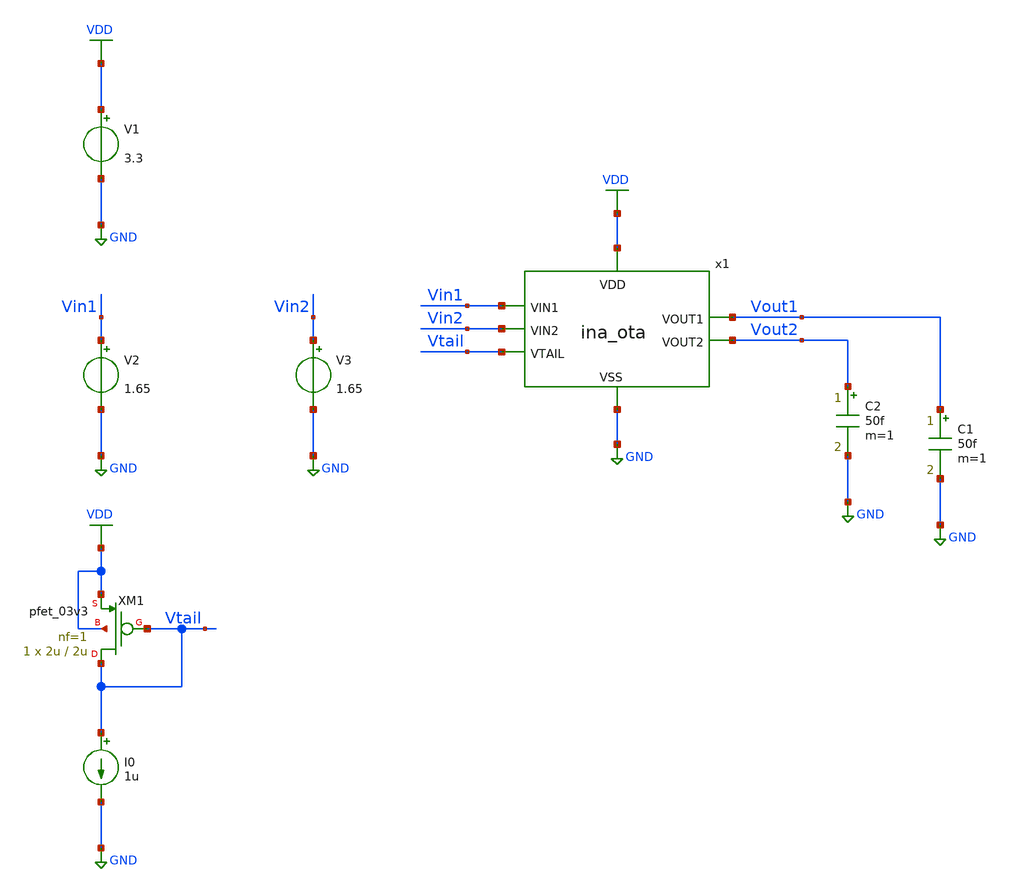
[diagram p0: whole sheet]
** sch_path: designs/libs/tb_ina/tb_ina_ota_ac/tb_ina_ota_ac.sch
**.subckt tb_ina_ota_ac
V1 VDD GND 3.3
V2 Vin1 GND 1.65
V3 Vin2 GND 1.65
C2 Vout2 GND 50f m=1
C1 Vout1 GND 50f m=1
XM1 Vtail Vtail VDD VDD pfet_03v3 L=2u W=2u nf=1 ad='int((nf+1)/2) * W/nf * 0.18u' as='int((nf+2)/2) * W/nf * 0.18u'
+ pd='2*int((nf+1)/2) * (W/nf + 0.18u)' ps='2*int((nf+2)/2) * (W/nf + 0.18u)' nrd='0.18u / W' nrs='0.18u / W'
+ sa=0 sb=0 sd=0 m=1
I0 Vtail GND 1u
x1 VDD Vtail Vin1 Vout2 Vout1 Vin2 GND ina_ota
**** begin user architecture code

.include $::180MCU_MODELS/design.ngspice
.lib $::180MCU_MODELS/sm141064.ngspice typical
.lib $::180MCU_MODELS/sm141064.ngspice cap_mim
.lib $::180MCU_MODELS/sm141064.ngspice moscap_typical
.lib $::180MCU_MODELS/sm141064.ngspice mimcap_typical
.lib $::180MCU_MODELS/sm141064.ngspice res_typical
* .lib $::180MCU_MODELS/sm141064.ngspice res_statistical
* ngspice commands




.control
save all

run
set color0 = white

*************************************
** PARAMETERS
*************************************

let Vdd  = 3.3
let Vcm  = 1.65
let Ibias = 1u

*************************************
** SOURCES
*************************************

alter @V1[DC] = $&Vdd
alter @V2[DC] = $&Vcm
alter @V3[DC] = $&Vcm
alter @V2[ACMAG] = 0.5
alter @V3[ACMAG] = -0.5
alter @I0[DC] = $&Ibias

*************************************
** AC SIMULATION
*************************************

ac dec 100 1 1G

*************************************
** MEASUREMENTS
*************************************

let vout_diff = v(Vout1)-v(Vout2)
let vin_diff  = v(Vin1)-v(Vin2)
let Av = vout_diff/vin_diff
let gain_db = db(Av)
let phase_deg = cph(Av)*180/pi
meas ac A0 FIND gain_db AT=1
let A0_3dB = A0 - 3
meas ac BW WHEN gain_db=A0_3dB
meas ac UGF WHEN gain_db=0
meas ac PHASE_UGF FIND phase_deg WHEN gain_db=0
let PM = PHASE_UGF
print PM

*************************************
** PLOTS
*************************************

plot gain_db
plot phase_deg

*************************************
** SAVE
*************************************

write tb_ina_ota_ac.raw


.endc
* ngspice commands



**** end user architecture code
**.ends

* expanding   symbol:  libs/core_ina/ina_ota/ina_ota.sym # of pins=7
** sym_path: designs/libs/core_ina/ina_ota/ina_ota.sym
** sch_path: designs/libs/core_ina/ina_ota/ina_ota.sch
.subckt ina_ota VDD VTAIL VIN1 VOUT2 VOUT1 VIN2 VSS
*.ipin Vin1
*.ipin Vin2
*.ipin Vtail
*.ipin VSS
*.opin Vout1
*.ipin VDD
*.opin Vout2
XM2 net4 net4 VDD VDD pfet_03v3 L=5u W=5u nf=1 ad='int((nf+1)/2) * W/nf * 0.18u' as='int((nf+2)/2) * W/nf * 0.18u'
+ pd='2*int((nf+1)/2) * (W/nf + 0.18u)' ps='2*int((nf+2)/2) * (W/nf + 0.18u)' nrd='0.18u / W' nrs='0.18u / W'
+ sa=0 sb=0 sd=0 m=1
XM1 net3 Vtail VDD VDD pfet_03v3 L=2u W=2u nf=1 ad='int((nf+1)/2) * W/nf * 0.18u' as='int((nf+2)/2) * W/nf * 0.18u'
+ pd='2*int((nf+1)/2) * (W/nf + 0.18u)' ps='2*int((nf+2)/2) * (W/nf + 0.18u)' nrd='0.18u / W' nrs='0.18u / W'
+ sa=0 sb=0 sd=0 m=20
XM3 net5 net5 VDD VDD pfet_03v3 L=5u W=5u nf=1 ad='int((nf+1)/2) * W/nf * 0.18u' as='int((nf+2)/2) * W/nf * 0.18u'
+ pd='2*int((nf+1)/2) * (W/nf + 0.18u)' ps='2*int((nf+2)/2) * (W/nf + 0.18u)' nrd='0.18u / W' nrs='0.18u / W'
+ sa=0 sb=0 sd=0 m=1
XM4 net1 Vin1 net3 VDD pfet_03v3 L=0.5u W=5u nf=1 ad='int((nf+1)/2) * W/nf * 0.18u' as='int((nf+2)/2) * W/nf * 0.18u'
+ pd='2*int((nf+1)/2) * (W/nf + 0.18u)' ps='2*int((nf+2)/2) * (W/nf + 0.18u)' nrd='0.18u / W' nrs='0.18u / W'
+ sa=0 sb=0 sd=0 m=1
XM5 net2 Vin2 net3 VDD pfet_03v3 L=0.5u W=5u nf=1 ad='int((nf+1)/2) * W/nf * 0.18u' as='int((nf+2)/2) * W/nf * 0.18u'
+ pd='2*int((nf+1)/2) * (W/nf + 0.18u)' ps='2*int((nf+2)/2) * (W/nf + 0.18u)' nrd='0.18u / W' nrs='0.18u / W'
+ sa=0 sb=0 sd=0 m=1
XM6 net4 net1 VSS VSS nfet_03v3 L=5u W=20u nf=1 ad='int((nf+1)/2) * W/nf * 0.18u' as='int((nf+2)/2) * W/nf * 0.18u'
+ pd='2*int((nf+1)/2) * (W/nf + 0.18u)' ps='2*int((nf+2)/2) * (W/nf + 0.18u)' nrd='0.18u / W' nrs='0.18u / W'
+ sa=0 sb=0 sd=0 m=1
XM7 net5 net2 VSS VSS nfet_03v3 L=5u W=20u nf=1 ad='int((nf+1)/2) * W/nf * 0.18u' as='int((nf+2)/2) * W/nf * 0.18u'
+ pd='2*int((nf+1)/2) * (W/nf + 0.18u)' ps='2*int((nf+2)/2) * (W/nf + 0.18u)' nrd='0.18u / W' nrs='0.18u / W'
+ sa=0 sb=0 sd=0 m=1
XM8 net1 net1 VSS VSS nfet_03v3 L=5u W=20u nf=1 ad='int((nf+1)/2) * W/nf * 0.18u' as='int((nf+2)/2) * W/nf * 0.18u'
+ pd='2*int((nf+1)/2) * (W/nf + 0.18u)' ps='2*int((nf+2)/2) * (W/nf + 0.18u)' nrd='0.18u / W' nrs='0.18u / W'
+ sa=0 sb=0 sd=0 m=1
XM9 net2 net2 VSS VSS nfet_03v3 L=5u W=20u nf=1 ad='int((nf+1)/2) * W/nf * 0.18u' as='int((nf+2)/2) * W/nf * 0.18u'
+ pd='2*int((nf+1)/2) * (W/nf + 0.18u)' ps='2*int((nf+2)/2) * (W/nf + 0.18u)' nrd='0.18u / W' nrs='0.18u / W'
+ sa=0 sb=0 sd=0 m=1
XM10 Vout1 net4 VDD VDD pfet_03v3 L=5u W=5u nf=1 ad='int((nf+1)/2) * W/nf * 0.18u' as='int((nf+2)/2) * W/nf * 0.18u'
+ pd='2*int((nf+1)/2) * (W/nf + 0.18u)' ps='2*int((nf+2)/2) * (W/nf + 0.18u)' nrd='0.18u / W' nrs='0.18u / W'
+ sa=0 sb=0 sd=0 m=1
XM11 Vout1 net2 VSS VSS nfet_03v3 L=5u W=20u nf=1 ad='int((nf+1)/2) * W/nf * 0.18u' as='int((nf+2)/2) * W/nf * 0.18u'
+ pd='2*int((nf+1)/2) * (W/nf + 0.18u)' ps='2*int((nf+2)/2) * (W/nf + 0.18u)' nrd='0.18u / W' nrs='0.18u / W'
+ sa=0 sb=0 sd=0 m=1
XM12 Vout2 net1 VSS VSS nfet_03v3 L=5u W=20u nf=1 ad='int((nf+1)/2) * W/nf * 0.18u' as='int((nf+2)/2) * W/nf * 0.18u'
+ pd='2*int((nf+1)/2) * (W/nf + 0.18u)' ps='2*int((nf+2)/2) * (W/nf + 0.18u)' nrd='0.18u / W' nrs='0.18u / W'
+ sa=0 sb=0 sd=0 m=1
XM13 Vout2 net5 VDD VDD pfet_03v3 L=5u W=5u nf=1 ad='int((nf+1)/2) * W/nf * 0.18u' as='int((nf+2)/2) * W/nf * 0.18u'
+ pd='2*int((nf+1)/2) * (W/nf + 0.18u)' ps='2*int((nf+2)/2) * (W/nf + 0.18u)' nrd='0.18u / W' nrs='0.18u / W'
+ sa=0 sb=0 sd=0 m=1
.ends

.GLOBAL GND
.GLOBAL VDD
.end
